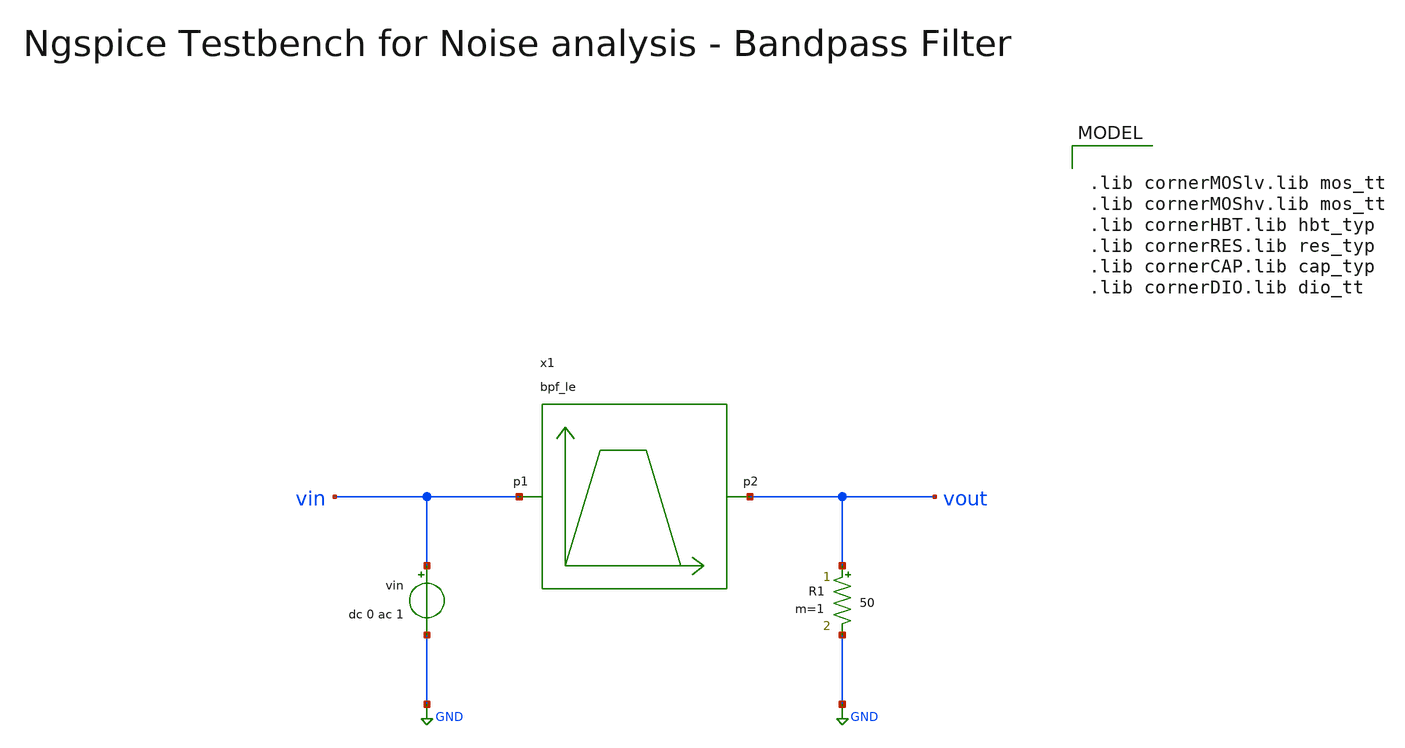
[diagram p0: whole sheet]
** sch_path: testbenches/xschem/two_port_tb_noise_ngspice.sch
**.subckt two_port_tb_noise_ngspice
x1 vin vout bpf_le
vin vin GND dc 0 ac 1
R1 vout GND 50 m=1
**** begin user architecture code


.include ../../../netlist/spice/bpf_le.spice
.param temp=27
.options savecurrents method=gear reltol=1e-3 abstol=1e-15 gmin=1e-15
.control

save all

set wr_vecnames
set wr_singlescale
set enable_noisy_r

* User Constants
let f_min = 120.0e9
let f_max = 200.0e9

* Operating Point Analysis
op
remzerovec
write @schname\.raw
set appendwrite

* Noise Analysis
noise v(vout) vin lin 1001 $&const.f_min $&const.f_max 1

* Plotting
setplot noise1
plot inoise_spectrum ylog ylabel 'Input Noise'
plot onoise_spectrum ylog ylabel 'Output Noise'
write @schname\.raw
set appendwrite

* Write Data
unset appendwrite
set wr_vecnames
set wr_singlescale
wrdata ../../../sim_data/@schname\.txt v(inoise_spectrum) v(onoise_spectrum)

* Measurements
setplot noise2
print inoise_total
print onoise_total

*quit
.endc



.lib cornerMOSlv.lib mos_tt
.lib cornerMOShv.lib mos_tt
.lib cornerHBT.lib hbt_typ
.lib cornerRES.lib res_typ
.lib cornerCAP.lib cap_typ
.lib cornerDIO.lib dio_tt

**** end user architecture code
**.ends
.GLOBAL GND
.end
